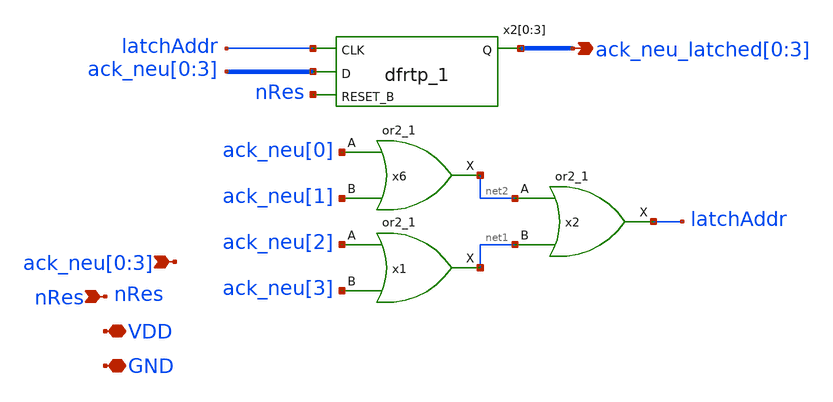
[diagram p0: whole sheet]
** sch_path: design/xschem/output_latch_4_neu.sch
**.subckt output_latch_4_neu ack_neu[0],ack_neu[1],ack_neu[2],ack_neu[3] nRes
*+ ack_neu_latched[0],ack_neu_latched[1],ack_neu_latched[2],ack_neu_latched[3] VDD GND
*.ipin ack_neu[0],ack_neu[1],ack_neu[2],ack_neu[3]
*.ipin nRes
*.opin ack_neu_latched[0],ack_neu_latched[1],ack_neu_latched[2],ack_neu_latched[3]
*.iopin VDD
*.iopin GND
x2[0] latchAddr ack_neu[0] nRes GND GND VDD VDD ack_neu_latched[0] sky130_fd_sc_hd__dfrtp_1
x2[1] latchAddr ack_neu[1] nRes GND GND VDD VDD ack_neu_latched[1] sky130_fd_sc_hd__dfrtp_1
x2[2] latchAddr ack_neu[2] nRes GND GND VDD VDD ack_neu_latched[2] sky130_fd_sc_hd__dfrtp_1
x2[3] latchAddr ack_neu[3] nRes GND GND VDD VDD ack_neu_latched[3] sky130_fd_sc_hd__dfrtp_1
x6 ack_neu[0] ack_neu[1] GND GND VDD VDD net2 sky130_fd_sc_hd__or2_1
x1 ack_neu[2] ack_neu[3] GND GND VDD VDD net1 sky130_fd_sc_hd__or2_1
x2 net2 net1 GND GND VDD VDD latchAddr sky130_fd_sc_hd__or2_1
**.ends
.end
